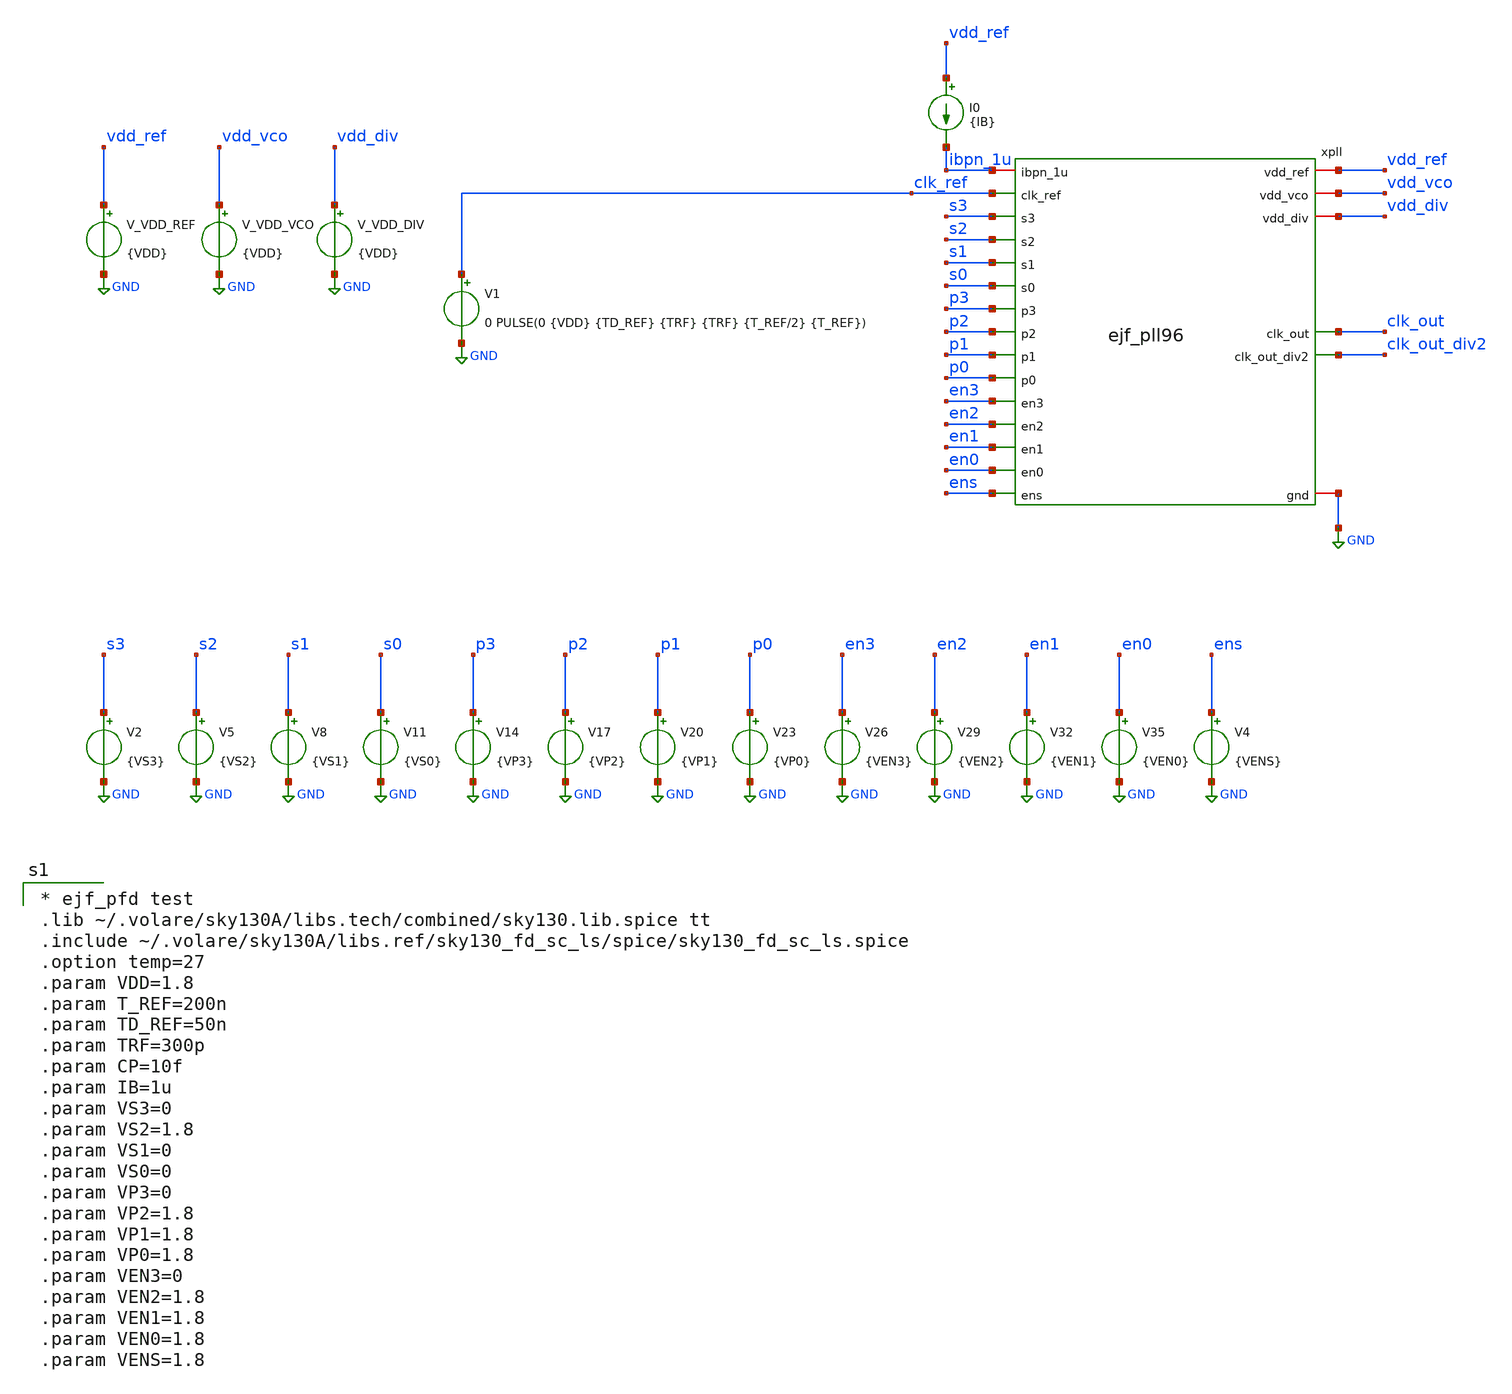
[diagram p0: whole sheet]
** sch_path: xschem/tb_ejf_pll96_top.sch
**.subckt tb_ejf_pll96_top
V_VDD_REF vdd_ref GND {VDD}
.save i(v_vdd_ref)
V1 clk_ref GND 0 PULSE(0 {VDD} {TD_REF} {TRF} {TRF} {T_REF/2} {T_REF})
I0 vdd_ref ibpn_1u {IB}
xpll vdd_vco vdd_div vdd_ref clk_ref s3 s2 s1 s0 p3 p2 clk_out p1 p0 en3 en2 en1 en0 ens GND ibpn_1u
+ clk_out_div2 ejf_pll96
V_VDD_VCO vdd_vco GND {VDD}
.save i(v_vdd_vco)
V_VDD_DIV vdd_div GND {VDD}
.save i(v_vdd_div)
V2 s3 GND {VS3}
V5 s2 GND {VS2}
V8 s1 GND {VS1}
V11 s0 GND {VS0}
V14 p3 GND {VP3}
V17 p2 GND {VP2}
V20 p1 GND {VP1}
V23 p0 GND {VP0}
V26 en3 GND {VEN3}
V29 en2 GND {VEN2}
V32 en1 GND {VEN1}
V35 en0 GND {VEN0}
V4 ens GND {VENS}
**** begin user architecture code

* ejf_pfd test
.lib ~/.volare/sky130A/libs.tech/combined/sky130.lib.spice tt
.include ~/.volare/sky130A/libs.ref/sky130_fd_sc_ls/spice/sky130_fd_sc_ls.spice
.option temp=27
.param VDD=1.8
.param T_REF=200n
.param TD_REF=50n
.param TRF=300p
.param CP=10f
.param IB=1u
.param VS3=0
.param VS2=1.8
.param VS1=0
.param VS0=0
.param VP3=0
.param VP2=1.8
.param VP1=1.8
.param VP0=1.8
.param VEN3=0
.param VEN2=1.8
.param VEN1=1.8
.param VEN0=1.8
.param VENS=1.8



* Run transient
* default reltol=1e-3 vntol=1e-6 abstol=1e-12
.options  reltol=1e-4 vntol=1e-7 abstol=1e-13
.options klu
.control
   save i(v_vdd_ref) i(v_vdd_vco) i(v_vdd_div)
   save clk_ref clk_out clk_out_div2
   save xpll.qref xpll.qref_b xpll.qclk xpll.qclk_b xpll.vc xpll.vco_outp xpll.vco_outn
   save xpll.xvco.vhi xpll.xvco.x0p xpll.xvco.x0n xpll.xvco.x1p xpll.xvco.x1n xpll.xvco.x2p
+ xpll.xvco.x2n xpll.xvco.x3p xpll.xvco.x3n
   tran 1n 10u
   write tb_ejf_pfd.raw
   meas tran i_v_vdd_avg avg i(v_vdd) from=0n to=10u
.endc
.end

**** end user architecture code
**.ends
.GLOBAL GND
.end
